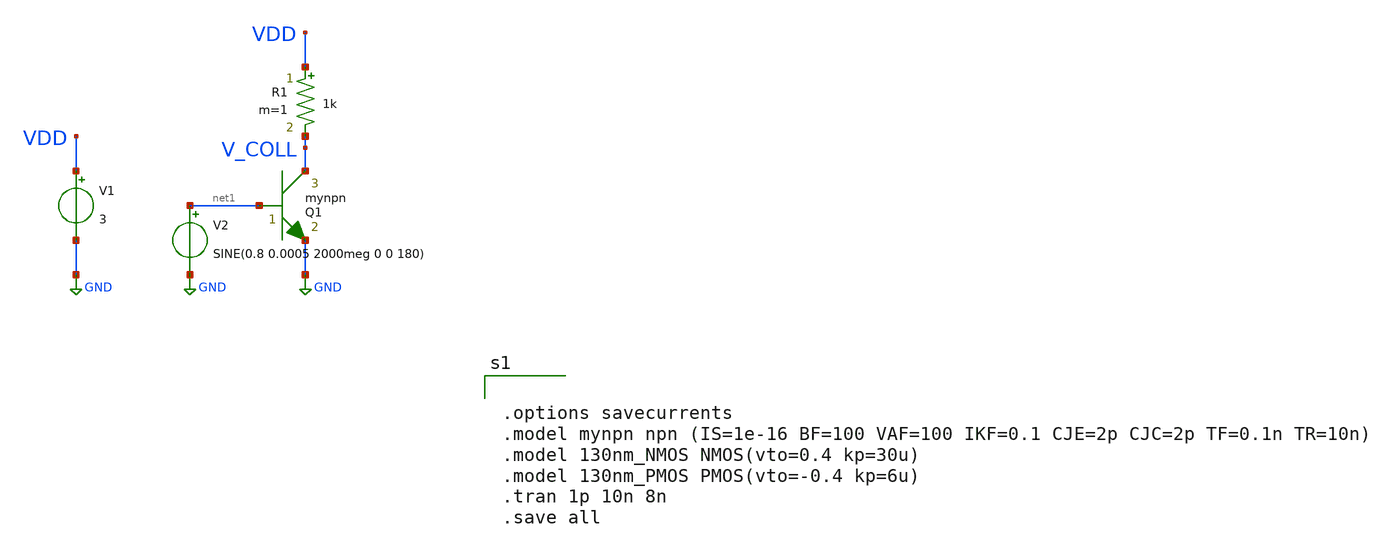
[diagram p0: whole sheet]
** sch_path: untitled-1.sch
**.subckt untitled-1
Q1 V_COLL net1 GND mynpn area=1 m=1
V1 VDD GND 3
R1 VDD V_COLL 1k m=1
V2 net1 GND SINE(0.8 0.0005 2000meg 0 0 180)
**** begin user architecture code


.options savecurrents
.model mynpn npn (IS=1e-16 BF=100 VAF=100 IKF=0.1 CJE=2p CJC=2p TF=0.1n TR=10n)
.model 130nm_NMOS NMOS(vto=0.4 kp=30u)
.model 130nm_PMOS PMOS(vto=-0.4 kp=6u)
.tran 1p 10n 8n
.save all




.include /usr/local/share/rad_modeling_blocks/rad_modeling_blocks.spice


**** end user architecture code
**.ends
.GLOBAL GND
.end
